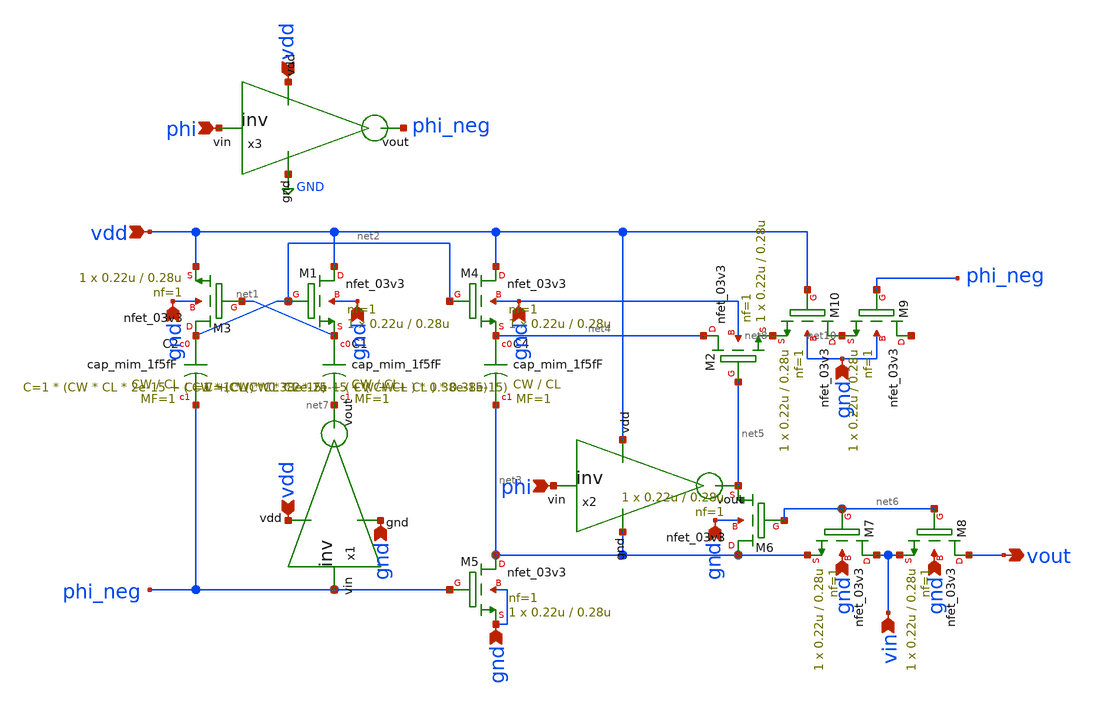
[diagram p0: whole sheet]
** sch_path: SAR_ADC/xschem/designs/bootstrap_sw.sch
**.subckt bootstrap_sw phi vdd vdd phi vin vout vdd gnd gnd gnd gnd gnd gnd gnd gnd gnd
*.ipin phi
*.ipin vdd
*.ipin vdd
*.ipin phi
*.ipin vin
*.opin vout
*.ipin vdd
*.ipin gnd
*.ipin gnd
*.ipin gnd
*.ipin gnd
*.ipin gnd
*.ipin gnd
*.ipin gnd
*.ipin gnd
*.ipin gnd
x1 vdd gnd net7 phi_neg inv cl=0.28u wp=0.44u wn=0.22u
XC1 net1 net7 sky130_fd_pr__cap_mim_1f5fF W=CW L=CL MF=1 m=1
XC2 net2 phi_neg sky130_fd_pr__cap_mim_1f5fF W=CW L=CL MF=1 m=1
XM1 vdd net2 net1 gnd sky130_fd_pr__nfet_03v3 L=0.28u W=0.22u nf=1 ad='int((nf+1)/2) * W/nf * 0.18u'
+ as='int((nf+2)/2) * W/nf * 0.18u' pd='2*int((nf+1)/2) * (W/nf + 0.18u)' ps='2*int((nf+2)/2) * (W/nf + 0.18u)'
+ nrd='0.18u / W' nrs='0.18u / W' sa=0 sb=0 sd=0 mult=1 m=1
XM4 vdd net2 net4 gnd sky130_fd_pr__nfet_03v3 L=0.28u W=0.22u nf=1 ad='int((nf+1)/2) * W/nf * 0.18u'
+ as='int((nf+2)/2) * W/nf * 0.18u' pd='2*int((nf+1)/2) * (W/nf + 0.18u)' ps='2*int((nf+2)/2) * (W/nf + 0.18u)'
+ nrd='0.18u / W' nrs='0.18u / W' sa=0 sb=0 sd=0 mult=1 m=1
XC4 net4 net3 sky130_fd_pr__cap_mim_1f5fF W=CW L=CL MF=1 m=1
XM5 net3 phi_neg gnd gnd sky130_fd_pr__nfet_03v3 L=0.28u W=0.22u nf=1 ad='int((nf+1)/2) * W/nf * 0.18u'
+ as='int((nf+2)/2) * W/nf * 0.18u' pd='2*int((nf+1)/2) * (W/nf + 0.18u)' ps='2*int((nf+2)/2) * (W/nf + 0.18u)'
+ nrd='0.18u / W' nrs='0.18u / W' sa=0 sb=0 sd=0 mult=1 m=1
x2 vdd net3 net5 phi inv cl=0.28u wp=0.44u wn=0.22u
x3 vdd GND phi_neg phi inv cl=0.28u wp=0.44u wn=0.22u
XM2 net4 net5 net8 gnd sky130_fd_pr__nfet_03v3 L=0.28u W=0.22u nf=1 ad='int((nf+1)/2) * W/nf * 0.18u'
+ as='int((nf+2)/2) * W/nf * 0.18u' pd='2*int((nf+1)/2) * (W/nf + 0.18u)' ps='2*int((nf+2)/2) * (W/nf + 0.18u)'
+ nrd='0.18u / W' nrs='0.18u / W' sa=0 sb=0 sd=0 mult=1 m=1
XM6 net3 net6 net5 gnd sky130_fd_pr__nfet_03v3 L=0.28u W=0.22u nf=1 ad='int((nf+1)/2) * W/nf * 0.18u'
+ as='int((nf+2)/2) * W/nf * 0.18u' pd='2*int((nf+1)/2) * (W/nf + 0.18u)' ps='2*int((nf+2)/2) * (W/nf + 0.18u)'
+ nrd='0.18u / W' nrs='0.18u / W' sa=0 sb=0 sd=0 mult=1 m=1
XM7 vin net6 net3 gnd sky130_fd_pr__nfet_03v3 L=0.28u W=0.22u nf=1 ad='int((nf+1)/2) * W/nf * 0.18u'
+ as='int((nf+2)/2) * W/nf * 0.18u' pd='2*int((nf+1)/2) * (W/nf + 0.18u)' ps='2*int((nf+2)/2) * (W/nf + 0.18u)'
+ nrd='0.18u / W' nrs='0.18u / W' sa=0 sb=0 sd=0 mult=1 m=1
XM8 vout net6 vin gnd sky130_fd_pr__nfet_03v3 L=0.28u W=0.22u nf=1 ad='int((nf+1)/2) * W/nf * 0.18u'
+ as='int((nf+2)/2) * W/nf * 0.18u' pd='2*int((nf+1)/2) * (W/nf + 0.18u)' ps='2*int((nf+2)/2) * (W/nf + 0.18u)'
+ nrd='0.18u / W' nrs='0.18u / W' sa=0 sb=0 sd=0 mult=1 m=1
XM9 net9 phi_neg net10 gnd sky130_fd_pr__nfet_03v3 L=0.28u W=0.22u nf=1 ad='int((nf+1)/2) * W/nf * 0.18u'
+ as='int((nf+2)/2) * W/nf * 0.18u' pd='2*int((nf+1)/2) * (W/nf + 0.18u)' ps='2*int((nf+2)/2) * (W/nf + 0.18u)'
+ nrd='0.18u / W' nrs='0.18u / W' sa=0 sb=0 sd=0 mult=1 m=1
XM10 net10 vdd net8 gnd sky130_fd_pr__nfet_03v3 L=0.28u W=0.22u nf=1 ad='int((nf+1)/2) * W/nf * 0.18u'
+ as='int((nf+2)/2) * W/nf * 0.18u' pd='2*int((nf+1)/2) * (W/nf + 0.18u)' ps='2*int((nf+2)/2) * (W/nf + 0.18u)'
+ nrd='0.18u / W' nrs='0.18u / W' sa=0 sb=0 sd=0 mult=1 m=1
XM3 net2 net1 vdd gnd sky130_fd_pr__nfet_03v3 L=0.28u W=0.22u nf=1 ad='int((nf+1)/2) * W/nf * 0.18u'
+ as='int((nf+2)/2) * W/nf * 0.18u' pd='2*int((nf+1)/2) * (W/nf + 0.18u)' ps='2*int((nf+2)/2) * (W/nf + 0.18u)'
+ nrd='0.18u / W' nrs='0.18u / W' sa=0 sb=0 sd=0 mult=1 m=1
**.ends

* expanding   symbol:  inv.sym # of pins=4
** sym_path: SAR_ADC/xschem/designs/inv.sym
** sch_path: SAR_ADC/xschem/designs/inv.sch
.subckt inv vdd gnd vout vin  cl=0.28u wp=0.44u wn=0.22u
*.ipin gnd
*.ipin vdd
*.ipin vin
*.opin vout
XM1 gnd vin vout gnd nfet_03v3 L=0.28u W=4u nf=1 ad='int((nf+1)/2) * W/nf * 0.18u' as='int((nf+2)/2) * W/nf * 0.18u'
+ pd='2*int((nf+1)/2) * (W/nf + 0.18u)' ps='2*int((nf+2)/2) * (W/nf + 0.18u)' nrd='0.18u / W' nrs='0.18u / W'
+ sa=0 sb=0 sd=0 m=1
XM2 vdd vin vout vdd pfet_03v3 L=0.28u W=4u nf=1 ad='int((nf+1)/2) * W/nf * 0.18u' as='int((nf+2)/2) * W/nf * 0.18u'
+ pd='2*int((nf+1)/2) * (W/nf + 0.18u)' ps='2*int((nf+2)/2) * (W/nf + 0.18u)' nrd='0.18u / W' nrs='0.18u / W'
+ sa=0 sb=0 sd=0 m=1
.ends

.GLOBAL GND
.end
